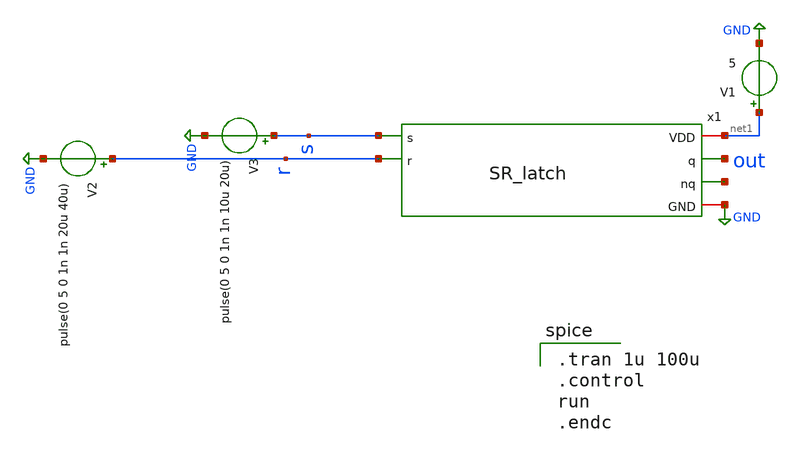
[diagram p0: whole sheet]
** sch_path: ADC/4bit_C2C/MagicAndSpice/SR_latch_TB.sch
**.subckt SR_latch_TB
V3 s GND pulse(0 5 0 1n 1n 10u 20u)
V1 net1 GND 5
x1 net1 out s net2 r GND SR_latch
V2 r GND pulse(0 5 0 1n 1n 20u 40u)
**** begin user architecture code

** opencircuitdesign pdks install
.lib $::SKYWATER_MODELS/sky130.lib.spice tt



.tran 1u 100u
.control
run
.endc

**** end user architecture code
**.ends
.GLOBAL GND
.end
